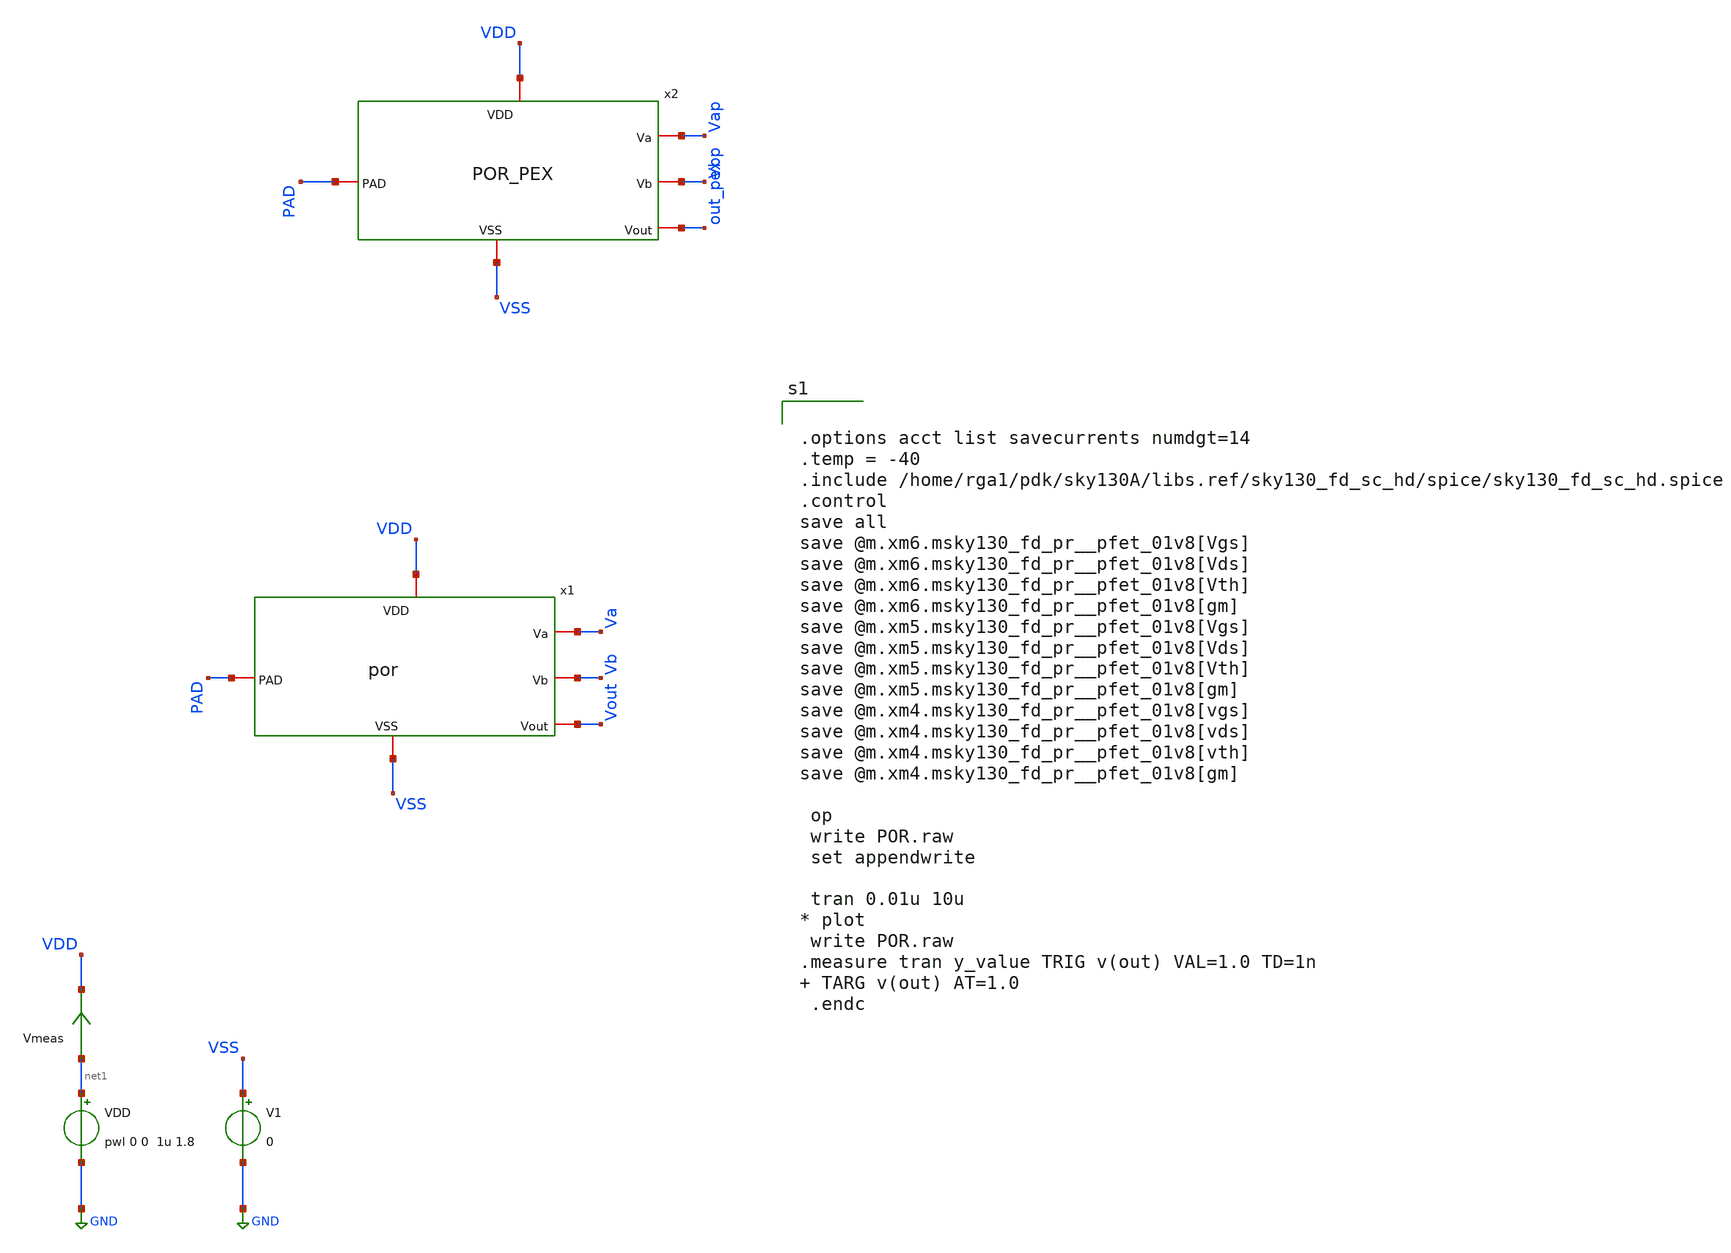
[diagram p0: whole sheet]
** sch_path: xschem/POR_TRAN.sch
**.subckt POR_TRAN
VDD net1 GND pwl 0 0 1u 1.8
V1 VSS GND 0
Vmeas net1 VDD 0
.save i(vmeas)
x1 VDD Va PAD Vb VSS Vout por
x2 VDD Vap PAD Vbp VSS out_pex POR_PEX
**** begin user architecture code

** opencircuitdesign pdks install
.lib $::SKYWATER_MODELS/sky130.lib.spice tt




.options acct list savecurrents numdgt=14
.temp = -40
.include /home/rga1/pdk/sky130A/libs.ref/sky130_fd_sc_hd/spice/sky130_fd_sc_hd.spice
.control
save all
save @m.xm6.msky130_fd_pr__pfet_01v8[Vgs]
save @m.xm6.msky130_fd_pr__pfet_01v8[Vds]
save @m.xm6.msky130_fd_pr__pfet_01v8[Vth]
save @m.xm6.msky130_fd_pr__pfet_01v8[gm]
save @m.xm5.msky130_fd_pr__pfet_01v8[Vgs]
save @m.xm5.msky130_fd_pr__pfet_01v8[Vds]
save @m.xm5.msky130_fd_pr__pfet_01v8[Vth]
save @m.xm5.msky130_fd_pr__pfet_01v8[gm]
save @m.xm4.msky130_fd_pr__pfet_01v8[vgs]
save @m.xm4.msky130_fd_pr__pfet_01v8[vds]
save @m.xm4.msky130_fd_pr__pfet_01v8[vth]
save @m.xm4.msky130_fd_pr__pfet_01v8[gm]

 op
 write POR.raw
 set appendwrite

 tran 0.01u 10u
* plot
 write POR.raw
.measure tran y_value TRIG v(out) VAL=1.0 TD=1n  TARG v(out) AT=1.0
 .endc


**** end user architecture code
**.ends
.GLOBAL GND
.end
